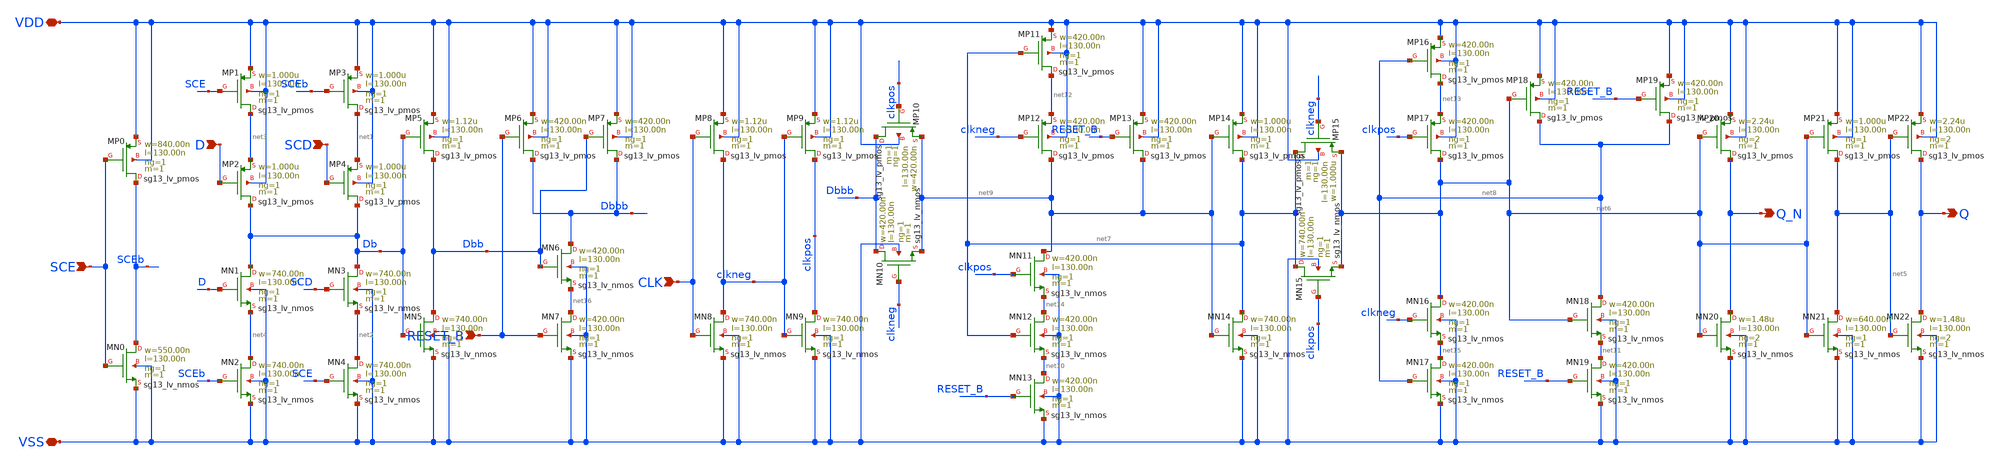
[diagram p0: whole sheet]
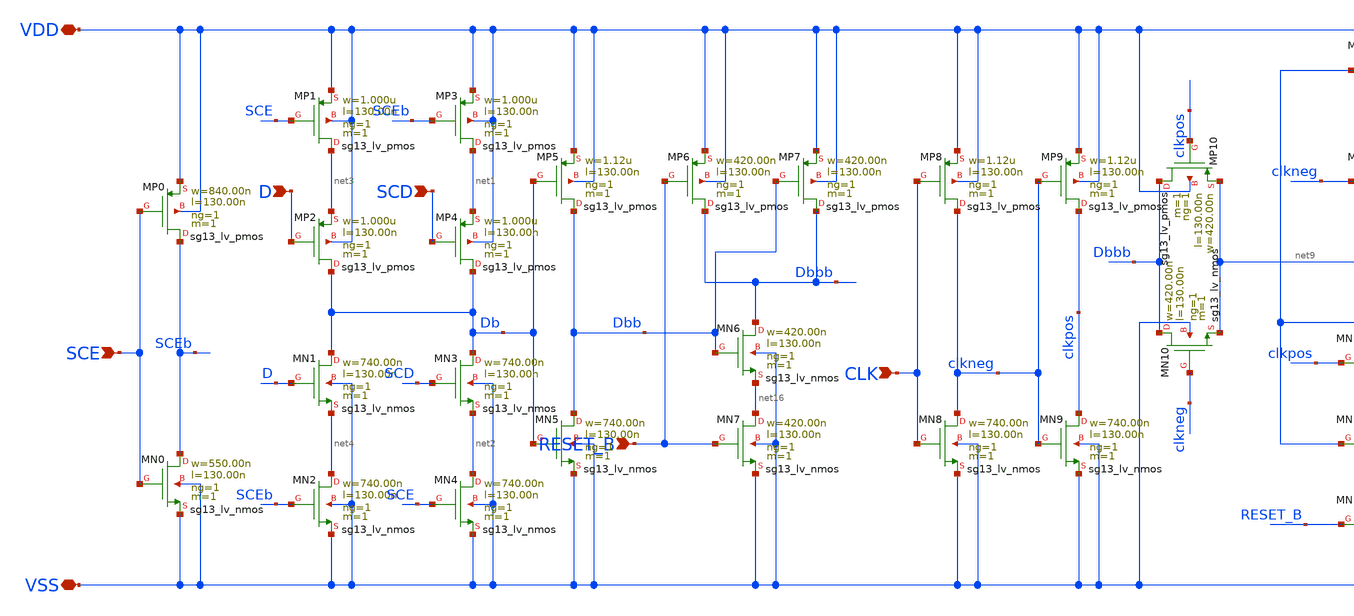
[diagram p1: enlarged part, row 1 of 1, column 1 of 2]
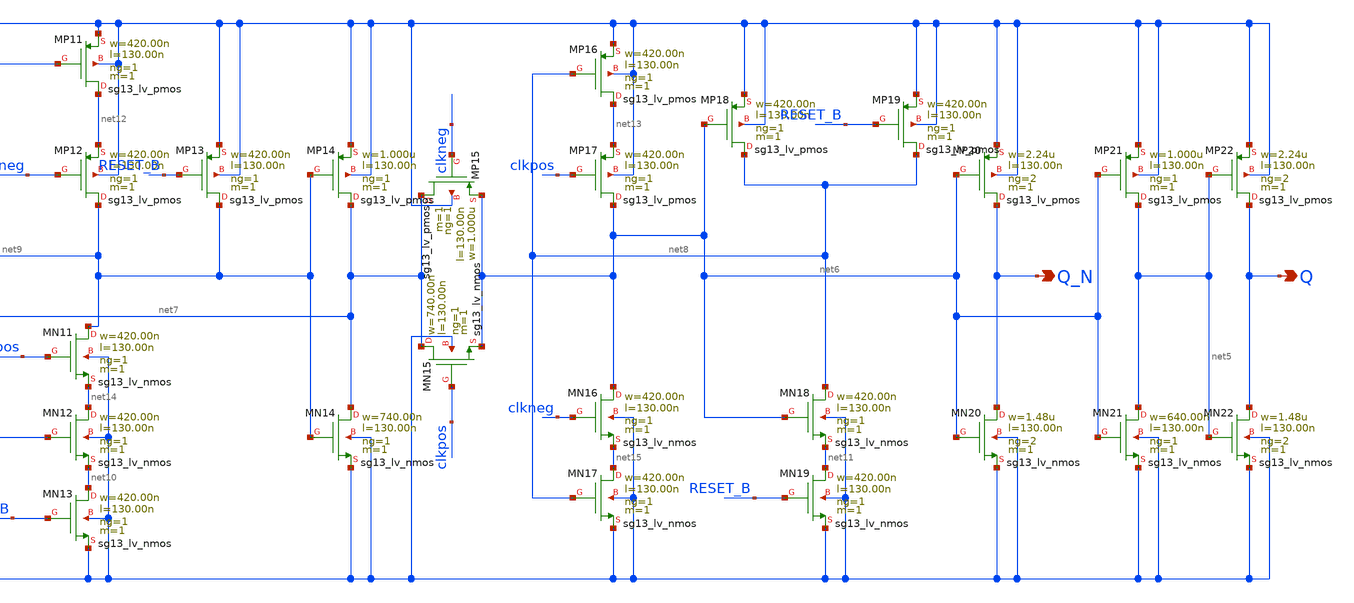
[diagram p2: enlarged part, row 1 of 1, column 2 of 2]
** sch_path: ihp-sg13g2/xschem_libs/sg13g2_stdcells/sg13g2_sdfrbp_2/schematic/sg13g2_sdfrbp_2.sch
* Copyright 2025 IHP PDK Authors
* Licensed under the Apache License, Version 2.0 (the "License");
* you may not use this file except in compliance with the License.
* You may obtain a copy of the License at
* https://www.apache.org/licenses/LICENSE-2.0
* Unless required by applicable law or agreed to in writing, software
* distributed under the License is distributed on an "AS IS" BASIS,
* WITHOUT WARRANTIES OR CONDITIONS OF ANY KIND, either express or implied.
* See the License for the specific language governing permissions and
* limitations under the License.
**.subckt sg13g2_sdfrbp_2 CLK VSS RESET_B Q_N Q SCE SCD D VDD
*.ipin CLK
*.iopin VSS
*.ipin RESET_B
*.opin Q_N
*.opin Q
*.ipin SCE
*.ipin SCD
*.ipin D
*.iopin VDD
XMP21 net5 net6 VDD VDD sg13_lv_pmos w=1.000u l=130.00n ng=1 m=1 mm_ok=1
XMP16 net13 net8 VDD VDD sg13_lv_pmos w=420.00n l=130.00n ng=1 m=1 mm_ok=1
XMP22 Q net5 VDD VDD sg13_lv_pmos w=2.24u l=130.00n ng=2 m=1 mm_ok=1
XMN21 net5 net6 VSS VSS sg13_lv_nmos w=640.00n l=130.00n ng=1 m=1 mm_ok=1
XMP15 net7 clkneg net6 VDD sg13_lv_pmos w=1.000u l=130.00n ng=1 m=1 mm_ok=1
XMN22 Q net5 VSS VSS sg13_lv_nmos w=1.48u l=130.00n ng=2 m=1 mm_ok=1
XMN9 clkpos clkneg VSS VSS sg13_lv_nmos w=740.00n l=130.00n ng=1 m=1 mm_ok=1
XMN15 net7 clkpos net6 VSS sg13_lv_nmos w=740.00n l=130.00n ng=1 m=1 mm_ok=1
XMP14 net7 net9 VDD VDD sg13_lv_pmos w=1.000u l=130.00n ng=1 m=1 mm_ok=1
XMN8 clkneg CLK VSS VSS sg13_lv_nmos w=740.00n l=130.00n ng=1 m=1 mm_ok=1
XMP9 clkpos clkneg VDD VDD sg13_lv_pmos w=1.12u l=130.00n ng=1 m=1 mm_ok=1
XMP8 clkneg CLK VDD VDD sg13_lv_pmos w=1.12u l=130.00n ng=1 m=1 mm_ok=1
XMN14 net7 net9 VSS VSS sg13_lv_nmos w=740.00n l=130.00n ng=1 m=1 mm_ok=1
XMP13 net9 RESET_B VDD VDD sg13_lv_pmos w=420.00n l=130.00n ng=1 m=1 mm_ok=1
XMP12 net9 clkneg net12 VDD sg13_lv_pmos w=420.00n l=130.00n ng=1 m=1 mm_ok=1
XMP11 net12 net7 VDD VDD sg13_lv_pmos w=420.00n l=130.00n ng=1 m=1 mm_ok=1
XMN13 net10 RESET_B VSS VSS sg13_lv_nmos w=420.00n l=130.00n ng=1 m=1 mm_ok=1
XMN12 net14 net7 net10 VSS sg13_lv_nmos w=420.00n l=130.00n ng=1 m=1 mm_ok=1
XMN11 net9 clkpos net14 VSS sg13_lv_nmos w=420.00n l=130.00n ng=1 m=1 mm_ok=1
XMP7 Dbbb Dbb VDD VDD sg13_lv_pmos w=420.00n l=130.00n ng=1 m=1 mm_ok=1
XMN10 Dbbb clkneg net9 VSS sg13_lv_nmos w=420.00n l=130.00n ng=1 m=1 mm_ok=1
XMP6 Dbbb RESET_B VDD VDD sg13_lv_pmos w=420.00n l=130.00n ng=1 m=1 mm_ok=1
XMN7 net16 RESET_B VSS VSS sg13_lv_nmos w=420.00n l=130.00n ng=1 m=1 mm_ok=1
XMN6 Dbbb Dbb net16 VSS sg13_lv_nmos w=420.00n l=130.00n ng=1 m=1 mm_ok=1
XMP10 Dbbb clkpos net9 VDD sg13_lv_pmos w=420.00n l=130.00n ng=1 m=1 mm_ok=1
XMN20 Q_N net6 VSS VSS sg13_lv_nmos w=1.48u l=130.00n ng=2 m=1 mm_ok=1
XMP20 Q_N net6 VDD VDD sg13_lv_pmos w=2.24u l=130.00n ng=2 m=1 mm_ok=1
XMN19 net11 RESET_B VSS VSS sg13_lv_nmos w=420.00n l=130.00n ng=1 m=1 mm_ok=1
XMN18 net8 net6 net11 VSS sg13_lv_nmos w=420.00n l=130.00n ng=1 m=1 mm_ok=1
XMP19 net8 RESET_B VDD VDD sg13_lv_pmos w=420.00n l=130.00n ng=1 m=1 mm_ok=1
XMP18 net8 net6 VDD VDD sg13_lv_pmos w=420.00n l=130.00n ng=1 m=1 mm_ok=1
XMN16 net6 clkneg net15 VSS sg13_lv_nmos w=420.00n l=130.00n ng=1 m=1 mm_ok=1
XMN17 net15 net8 VSS VSS sg13_lv_nmos w=420.00n l=130.00n ng=1 m=1 mm_ok=1
XMP17 net6 clkpos net13 VDD sg13_lv_pmos w=420.00n l=130.00n ng=1 m=1 mm_ok=1
XMN5 Dbb Db VSS VSS sg13_lv_nmos w=740.00n l=130.00n ng=1 m=1 mm_ok=1
XMP5 Dbb Db VDD VDD sg13_lv_pmos w=1.12u l=130.00n ng=1 m=1 mm_ok=1
XMN2 net4 SCEb VSS VSS sg13_lv_nmos w=740.00n l=130.00n ng=1 m=1 mm_ok=1
XMN4 net2 SCE VSS VSS sg13_lv_nmos w=740.00n l=130.00n ng=1 m=1 mm_ok=1
XMN0 SCEb SCE VSS VSS sg13_lv_nmos w=550.00n l=130.00n ng=1 m=1 mm_ok=1
XMN1 Db D net4 VSS sg13_lv_nmos w=740.00n l=130.00n ng=1 m=1 mm_ok=1
XMN3 Db SCD net2 VSS sg13_lv_nmos w=740.00n l=130.00n ng=1 m=1 mm_ok=1
XMP2 Db D net3 VDD sg13_lv_pmos w=1.000u l=130.00n ng=1 m=1 mm_ok=1
XMP4 Db SCD net1 VDD sg13_lv_pmos w=1.000u l=130.00n ng=1 m=1 mm_ok=1
XMP0 SCEb SCE VDD VDD sg13_lv_pmos w=840.00n l=130.00n ng=1 m=1 mm_ok=1
XMP3 net1 SCEb VDD VDD sg13_lv_pmos w=1.000u l=130.00n ng=1 m=1 mm_ok=1
XMP1 net3 SCE VDD VDD sg13_lv_pmos w=1.000u l=130.00n ng=1 m=1 mm_ok=1
**.ends
.end
